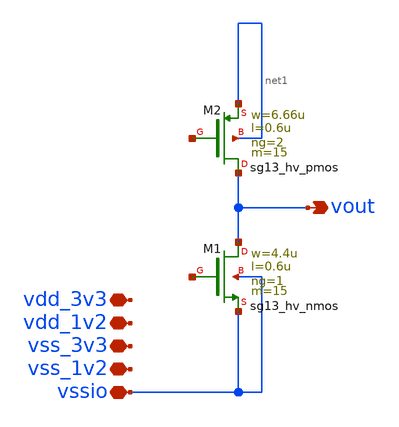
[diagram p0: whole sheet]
** sch_path: macros/outbuffer/schematic/xschem/outbuffer.sch
**.subckt outbuffer vdd_3v3 vdd_1v2 vss_3v3 vss_1v2 vssio vout
*.iopin vdd_3v3
*.iopin vdd_1v2
*.iopin vss_3v3
*.iopin vss_1v2
*.iopin vssio
*.opin vout
XM1 vout net2 vssio vssio sg13_hv_nmos w=4.4u l=0.6u ng=1 m=15 mm_ok=1
XM2 vout net3 net1 net1 sg13_hv_pmos w=6.66u l=0.6u ng=2 m=15 mm_ok=1
**.ends
.end
